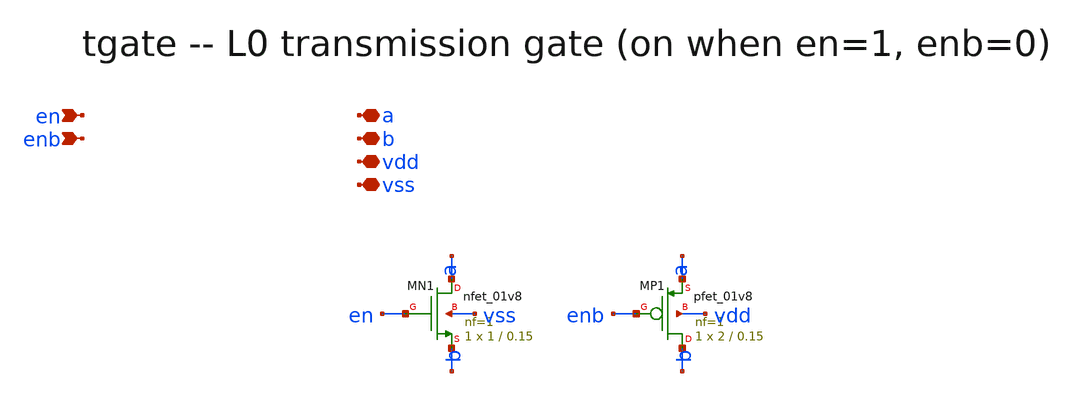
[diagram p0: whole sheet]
** sch_path: xschem/onetops/tgate.sch
**.subckt tgate en enb a b vdd vss
*.ipin en
*.ipin enb
*.iopin a
*.iopin b
*.iopin vdd
*.iopin vss
XMN1 a en b vss sky130_fd_pr__nfet_01v8 L=0.15 W=1 nf=1 ad='int((1 + 1)/2) * 1 / 1 * 0.29' as='int((1 + 2)/2) * 1 / 1 * 0.29'
+ pd='2*int((1 + 1)/2) * (1 / 1 + 0.29)' ps='2*int((1 + 2)/2) * (1 / 1 + 0.29)' nrd='0.29 / 1 ' nrs='0.29 / 1 '
+ sa=0 sb=0 sd=0 mult=1 m=1
XMP1 b enb a vdd sky130_fd_pr__pfet_01v8 L=0.15 W=2 nf=1 ad='int((1 + 1)/2) * 2 / 1 * 0.29' as='int((1 + 2)/2) * 2 / 1 * 0.29'
+ pd='2*int((1 + 1)/2) * (2 / 1 + 0.29)' ps='2*int((1 + 2)/2) * (2 / 1 + 0.29)' nrd='0.29 / 2 ' nrs='0.29 / 2 '
+ sa=0 sb=0 sd=0 mult=1 m=1
**.ends
.end
